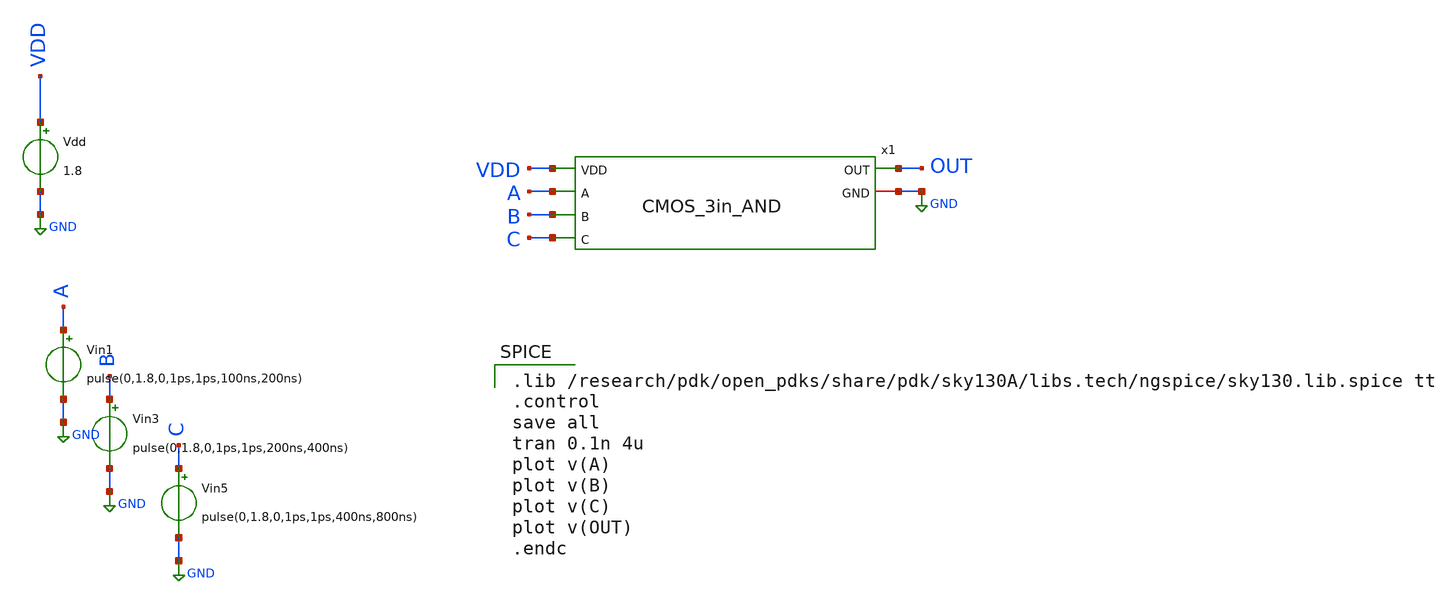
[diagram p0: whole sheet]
** sch_path: skywater_stuff/CMOS_3in_AND_sim.sch
**.subckt CMOS_3in_AND_sim
Vin1 A GND pulse(0,1.8,0,1ps,1ps,100ns,200ns)
Vin3 B GND pulse(0,1.8,0,1ps,1ps,200ns,400ns)
Vin5 C GND pulse(0,1.8,0,1ps,1ps,400ns,800ns)
Vdd VDD GND 1.8
x1 A B C OUT GND VDD CMOS_3in_AND
**** begin user architecture code

.lib /research/pdk/open_pdks/share/pdk/sky130A/libs.tech/ngspice/sky130.lib.spice tt
.control
save all
tran 0.1n 4u
plot v(A)
plot v(B)
plot v(C)
plot v(OUT)
.endc


**** end user architecture code
**.ends

* expanding   symbol:  CMOS_3in_AND.sym # of pins=6
** sym_path: skywater_stuff/CMOS_3in_AND.sym
** sch_path: skywater_stuff/CMOS_3in_AND.sch
.subckt CMOS_3in_AND A B C OUT GND VDD
*.ipin A
*.ipin B
*.ipin C
*.opin OUT
*.iopin GND
*.ipin VDD
XM3 net1 B VDD VDD sky130_fd_pr__pfet_01v8 L=0.15 W=3 nf=1 ad='int((nf+1)/2) * W/nf * 0.29' as='int((nf+2)/2) * W/nf * 0.29'
+ pd='2*int((nf+1)/2) * (W/nf + 0.29)' ps='2*int((nf+2)/2) * (W/nf + 0.29)' nrd='0.29 / W' nrs='0.29 / W'
+ sa=0 sb=0 sd=0 mult=1 m=1
XM4 net1 C VDD VDD sky130_fd_pr__pfet_01v8 L=0.15 W=3 nf=1 ad='int((nf+1)/2) * W/nf * 0.29' as='int((nf+2)/2) * W/nf * 0.29'
+ pd='2*int((nf+1)/2) * (W/nf + 0.29)' ps='2*int((nf+2)/2) * (W/nf + 0.29)' nrd='0.29 / W' nrs='0.29 / W'
+ sa=0 sb=0 sd=0 mult=1 m=1
XM6 net2 B net3 GND sky130_fd_pr__nfet_01v8 L=0.15 W=1.5 nf=1 ad='int((nf+1)/2) * W/nf * 0.29' as='int((nf+2)/2) * W/nf * 0.29'
+ pd='2*int((nf+1)/2) * (W/nf + 0.29)' ps='2*int((nf+2)/2) * (W/nf + 0.29)' nrd='0.29 / W' nrs='0.29 / W'
+ sa=0 sb=0 sd=0 mult=1 m=1
XM7 net3 C GND GND sky130_fd_pr__nfet_01v8 L=0.15 W=1.5 nf=1 ad='int((nf+1)/2) * W/nf * 0.29' as='int((nf+2)/2) * W/nf * 0.29'
+ pd='2*int((nf+1)/2) * (W/nf + 0.29)' ps='2*int((nf+2)/2) * (W/nf + 0.29)' nrd='0.29 / W' nrs='0.29 / W'
+ sa=0 sb=0 sd=0 mult=1 m=1
XM9 OUT net1 GND GND sky130_fd_pr__nfet_01v8 L=0.15 W=1.5 nf=1 ad='int((nf+1)/2) * W/nf * 0.29' as='int((nf+2)/2) * W/nf * 0.29'
+ pd='2*int((nf+1)/2) * (W/nf + 0.29)' ps='2*int((nf+2)/2) * (W/nf + 0.29)' nrd='0.29 / W' nrs='0.29 / W'
+ sa=0 sb=0 sd=0 mult=1 m=1
XM10 OUT net1 VDD VDD sky130_fd_pr__pfet_01v8 L=0.15 W=3 nf=1 ad='int((nf+1)/2) * W/nf * 0.29' as='int((nf+2)/2) * W/nf * 0.29'
+ pd='2*int((nf+1)/2) * (W/nf + 0.29)' ps='2*int((nf+2)/2) * (W/nf + 0.29)' nrd='0.29 / W' nrs='0.29 / W'
+ sa=0 sb=0 sd=0 mult=1 m=1
XM1 net1 A net2 GND sky130_fd_pr__nfet_01v8 L=0.15 W=1.5 nf=1 ad='int((nf+1)/2) * W/nf * 0.29' as='int((nf+2)/2) * W/nf * 0.29'
+ pd='2*int((nf+1)/2) * (W/nf + 0.29)' ps='2*int((nf+2)/2) * (W/nf + 0.29)' nrd='0.29 / W' nrs='0.29 / W'
+ sa=0 sb=0 sd=0 mult=1 m=1
XM2 net1 A VDD VDD sky130_fd_pr__pfet_01v8 L=0.15 W=3 nf=1 ad='int((nf+1)/2) * W/nf * 0.29' as='int((nf+2)/2) * W/nf * 0.29'
+ pd='2*int((nf+1)/2) * (W/nf + 0.29)' ps='2*int((nf+2)/2) * (W/nf + 0.29)' nrd='0.29 / W' nrs='0.29 / W'
+ sa=0 sb=0 sd=0 mult=1 m=1
.ends

.GLOBAL GND
.end
